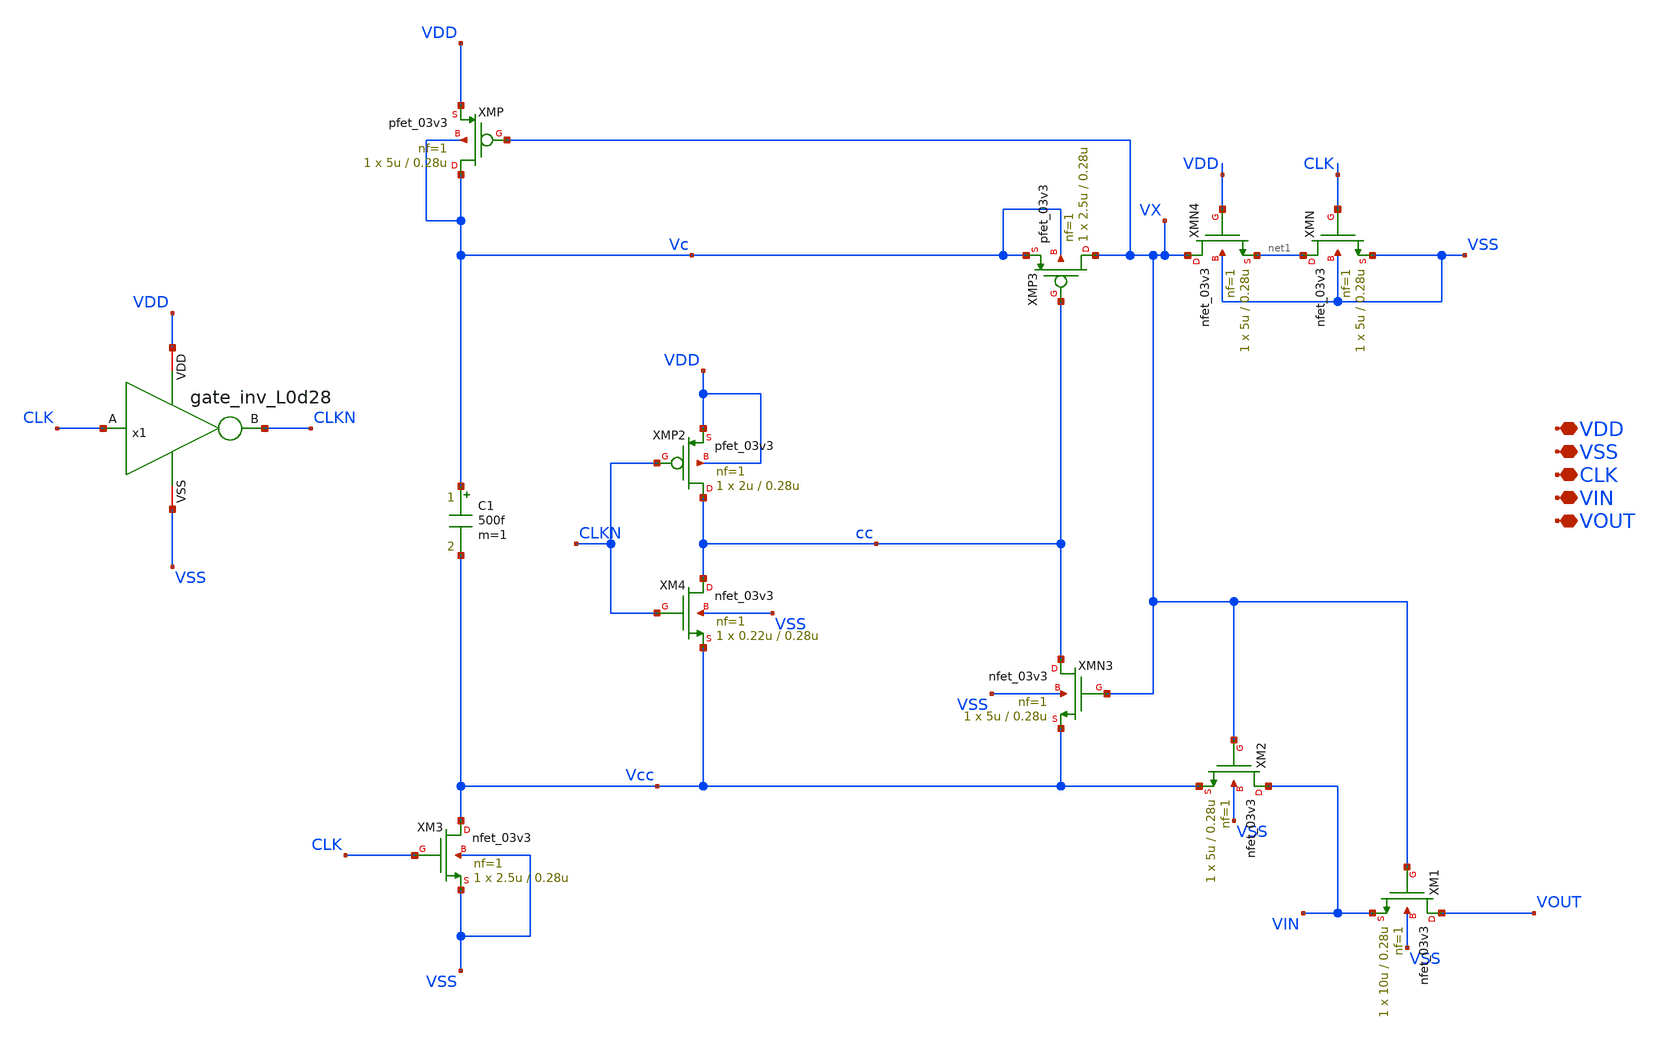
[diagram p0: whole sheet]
** sch_path: designs/sar_adc/samplehold/bootstrapped/xschem/bootstrapped.sch
**.subckt bootstrapped CLK VSS VDD VOUT VIN
*.iopin CLK
*.iopin VSS
*.iopin VDD
*.iopin VOUT
*.iopin VIN
XMN net1 CLK VSS VSS nfet_03v3 L=0.28u W=5u nf=1 ad='int((nf+1)/2) * W/nf * 0.18u' as='int((nf+2)/2) * W/nf * 0.18u'
+ pd='2*int((nf+1)/2) * (W/nf + 0.18u)' ps='2*int((nf+2)/2) * (W/nf + 0.18u)' nrd='0.18u / W' nrs='0.18u / W'
+ sa=0 sb=0 sd=0 m=1
XMP2 cc CLKN VDD VDD pfet_03v3 L=0.28u W=2u nf=1 ad='int((nf+1)/2) * W/nf * 0.18u' as='int((nf+2)/2) * W/nf * 0.18u'
+ pd='2*int((nf+1)/2) * (W/nf + 0.18u)' ps='2*int((nf+2)/2) * (W/nf + 0.18u)' nrd='0.18u / W' nrs='0.18u / W'
+ sa=0 sb=0 sd=0 m=1
XMN3 cc VX Vcc VSS nfet_03v3 L=0.28u W=5u nf=1 ad='int((nf+1)/2) * W/nf * 0.18u' as='int((nf+2)/2) * W/nf * 0.18u'
+ pd='2*int((nf+1)/2) * (W/nf + 0.18u)' ps='2*int((nf+2)/2) * (W/nf + 0.18u)' nrd='0.18u / W' nrs='0.18u / W'
+ sa=0 sb=0 sd=0 m=1
XMP3 VX cc Vc Vc pfet_03v3 L=0.28u W=2.5u nf=1 ad='int((nf+1)/2) * W/nf * 0.18u' as='int((nf+2)/2) * W/nf * 0.18u'
+ pd='2*int((nf+1)/2) * (W/nf + 0.18u)' ps='2*int((nf+2)/2) * (W/nf + 0.18u)' nrd='0.18u / W' nrs='0.18u / W'
+ sa=0 sb=0 sd=0 m=1
XMN4 VX VDD net1 VSS nfet_03v3 L=0.28u W=5u nf=1 ad='int((nf+1)/2) * W/nf * 0.18u' as='int((nf+2)/2) * W/nf * 0.18u'
+ pd='2*int((nf+1)/2) * (W/nf + 0.18u)' ps='2*int((nf+2)/2) * (W/nf + 0.18u)' nrd='0.18u / W' nrs='0.18u / W'
+ sa=0 sb=0 sd=0 m=1
x1 VDD CLKN CLK VSS gate_inv_L0d28
XMP Vc VX VDD Vc pfet_03v3 L=0.28u W=5u nf=1 ad='int((nf+1)/2) * W/nf * 0.18u' as='int((nf+2)/2) * W/nf * 0.18u'
+ pd='2*int((nf+1)/2) * (W/nf + 0.18u)' ps='2*int((nf+2)/2) * (W/nf + 0.18u)' nrd='0.18u / W' nrs='0.18u / W'
+ sa=0 sb=0 sd=0 m=1
C1 Vc Vcc 500f m=1
XM1 VOUT VX VIN VSS nfet_03v3 L=0.28u W=10u nf=1 ad='int((nf+1)/2) * W/nf * 0.18u' as='int((nf+2)/2) * W/nf * 0.18u'
+ pd='2*int((nf+1)/2) * (W/nf + 0.18u)' ps='2*int((nf+2)/2) * (W/nf + 0.18u)' nrd='0.18u / W' nrs='0.18u / W'
+ sa=0 sb=0 sd=0 m=1
XM2 VIN VX Vcc VSS nfet_03v3 L=0.28u W=5u nf=1 ad='int((nf+1)/2) * W/nf * 0.18u' as='int((nf+2)/2) * W/nf * 0.18u'
+ pd='2*int((nf+1)/2) * (W/nf + 0.18u)' ps='2*int((nf+2)/2) * (W/nf + 0.18u)' nrd='0.18u / W' nrs='0.18u / W'
+ sa=0 sb=0 sd=0 m=1
XM3 Vcc CLK VSS VSS nfet_03v3 L=0.28u W=2.5u nf=1 ad='int((nf+1)/2) * W/nf * 0.18u' as='int((nf+2)/2) * W/nf * 0.18u'
+ pd='2*int((nf+1)/2) * (W/nf + 0.18u)' ps='2*int((nf+2)/2) * (W/nf + 0.18u)' nrd='0.18u / W' nrs='0.18u / W'
+ sa=0 sb=0 sd=0 m=1
XM4 cc CLKN Vcc VSS nfet_03v3 L=0.28u W=0.22u nf=1 ad='int((nf+1)/2) * W/nf * 0.18u' as='int((nf+2)/2) * W/nf * 0.18u'
+ pd='2*int((nf+1)/2) * (W/nf + 0.18u)' ps='2*int((nf+2)/2) * (W/nf + 0.18u)' nrd='0.18u / W' nrs='0.18u / W'
+ sa=0 sb=0 sd=0 m=1
**.ends

* expanding   symbol:  sar_adc/samplehold/gate_inv_L0d28/xschem/gate_inv_L0d28.sym # of pins=4
** sym_path: sar_adc/samplehold/gate_inv_L0d28/xschem/gate_inv_L0d28.sym
** sch_path: sar_adc/samplehold/gate_inv_L0d28/xschem/gate_inv_L0d28.sch
.subckt gate_inv_L0d28 VDD B A VSS
*.opin B
*.ipin A
*.iopin VDD
*.iopin VSS
XMN B A VSS VSS nfet_03v3 L=0.28u W=1u nf=1 ad='int((nf+1)/2) * W/nf * 0.18u' as='int((nf+2)/2) * W/nf * 0.18u'
+ pd='2*int((nf+1)/2) * (W/nf + 0.18u)' ps='2*int((nf+2)/2) * (W/nf + 0.18u)' nrd='0.18u / W' nrs='0.18u / W'
+ sa=0 sb=0 sd=0 m=2
XMP B A VDD VDD pfet_03v3 L=0.28u W=3u nf=1 ad='int((nf+1)/2) * W/nf * 0.18u' as='int((nf+2)/2) * W/nf * 0.18u'
+ pd='2*int((nf+1)/2) * (W/nf + 0.18u)' ps='2*int((nf+2)/2) * (W/nf + 0.18u)' nrd='0.18u / W' nrs='0.18u / W'
+ sa=0 sb=0 sd=0 m=2
.ends

.end
